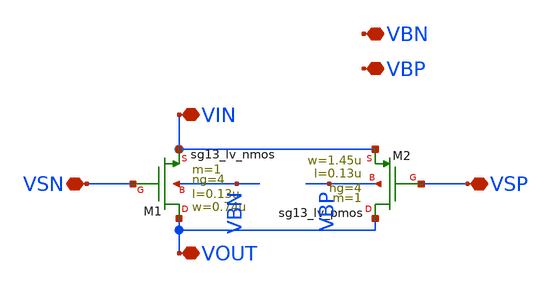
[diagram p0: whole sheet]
** sch_path: transmission_gate.sch
**.subckt transmission_gate VIN VSN VOUT VSP VBN VBP
*.iopin VIN
*.iopin VSN
*.iopin VOUT
*.iopin VSP
*.iopin VBN
*.iopin VBP
XM1 VOUT VSN VIN VBN sg13_lv_nmos w=0.74u l=0.13u ng=4 m=1 mm_ok=1
XM2 VOUT VSP VIN VBP sg13_lv_pmos w=1.45u l=0.13u ng=4 m=1 mm_ok=1
**.ends
.end
